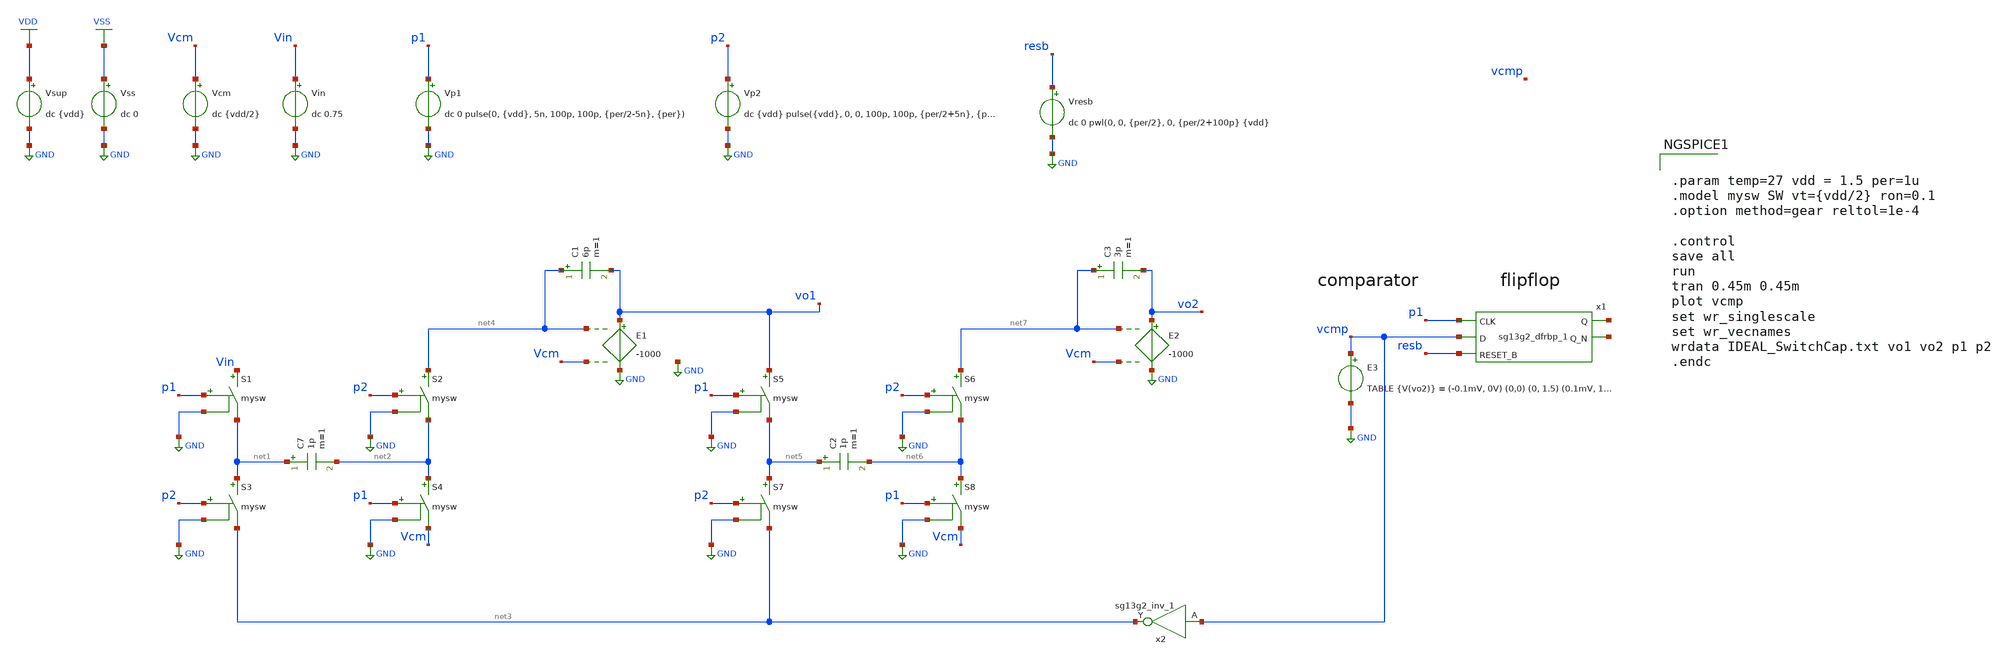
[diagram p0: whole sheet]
** sch_path: DSM/Schematics/Designs_Hrishi/IdealCircuits/IDEAL_DSM_VCCS.sch
**.subckt IDEAL_DSM_VCCS
Vcm Vcm GND dc {vdd/2}
Vin Vin GND dc 0.75
Vp1 p1 GND dc 0 pulse(0, {vdd}, 5n, 100p, 100p, {per/2-5n}, {per})
Vp2 p2 GND dc {vdd} pulse({vdd}, 0, 0, 100p, 100p, {per/2+5n}, {per})
S1 Vin net1 p1 GND mysw
S2 net4 net2 p2 GND mysw
S3 net1 net3 p2 GND mysw
S4 net2 Vcm p1 GND mysw
C7 net1 net2 1p m=1
C1 net4 vo1 6p m=1
S5 vo1 net5 p1 GND mysw
S6 net7 net6 p2 GND mysw
S7 net5 net3 p2 GND mysw
S8 net6 Vcm p1 GND mysw
C2 net5 net6 1p m=1
C3 net7 vo2 3p m=1
x2 net3 vcmp Vdd Vss sg13g2_inv_1
Vresb resb GND dc 0 pwl(0, 0, {per/2}, 0, {per/2+100p} {vdd}
Vsup VDD GND dc {vdd}
Vss VSS GND dc 0
E1 vo1 GND net4 Vcm -1000
E2 vo2 GND net7 Vcm -1000
E3 vcmp GND TABLE {V(vo2)} = (-0.1mV, 0V) (0,0) (0, 1.5) (0.1mV, 1.5)
x1 net8 net9 p1 vcmp resb VDD VSS sg13g2_dfrbp_1
**** begin user architecture code

.lib $::SG13G2_MODELS/cornerMOSlv.lib mos_tt
.lib $::SG13G2_MODELS/cornerRES.lib res_typ
.inc /foss/pdks/sg13g2/libs.ref/sg13g2_stdcell/spice/sg13g2_stdcell.spice



.param temp=27 vdd = 1.5 per=1u
.model mysw SW vt={vdd/2} ron=0.1
.option method=gear reltol=1e-4

.control
save all
run
tran 0.45m 0.45m
plot vcmp
set wr_singlescale
set wr_vecnames
wrdata IDEAL_SwitchCap.txt vo1 vo2 p1 p2
.endc


**** end user architecture code
**.ends

* expanding   symbol:  sg13g2_stdcells/sg13g2_inv_1.sym # of pins=2
** sym_path: sg13g2_stdcells/sg13g2_inv_1.sym
** sch_path: sg13g2_stdcells/sg13g2_inv_1.sch
.subckt sg13g2_inv_1 Y A VDD VSS
*.opin Y
*.ipin A
*.iopin VDD
*.iopin VSS
XM1 Y A VSS VSS sg13_lv_nmos w=740.00n l=130.00n ng=1 m=1 mm_ok=1
XM2 Y A VDD VDD sg13_lv_pmos w=1.12u l=130.00n ng=1 m=1 mm_ok=1
.ends


* expanding   symbol:  sg13g2_stdcells/sg13g2_dfrbp_1.sym # of pins=5
** sym_path: sg13g2_stdcells/sg13g2_dfrbp_1.sym
** sch_path: sg13g2_stdcells/sg13g2_dfrbp_1.sch
.subckt sg13g2_dfrbp_1 Q Q_N CLK D RESET_B VDD VSS
*.ipin D
*.ipin RESET_B
*.ipin CLK
*.opin Q
*.opin Q_N
*.iopin VDD
*.iopin VSS
XM1 Db D net10 VSS sg13_lv_nmos w=420.00n l=130.00n ng=1 m=1 mm_ok=1
XM2 net10 RESET_B VSS VSS sg13_lv_nmos w=420.00n l=130.00n ng=1 m=1 mm_ok=1
XM3 net1 clkneg net9 VSS sg13_lv_nmos w=420.00n l=130.00n ng=1 m=1 mm_ok=1
XM4 net9 net1 VSS VSS sg13_lv_nmos w=420.00n l=130.00n ng=1 m=1 mm_ok=1
XM5 net1 net1 net5 VSS sg13_lv_nmos w=420.00n l=130.00n ng=1 m=1 mm_ok=1
XM6 net5 RESET_B VSS VSS sg13_lv_nmos w=420.00n l=130.00n ng=1 m=1 mm_ok=1
XM7 Q_N net1 VSS VSS sg13_lv_nmos w=740.00n l=130.00n ng=1 m=1 mm_ok=1
XM8 net2 net1 VSS VSS sg13_lv_nmos w=740.00n l=130.00n ng=1 m=1 mm_ok=1
XM9 Q net2 VSS VSS sg13_lv_nmos w=740.00n l=130.00n ng=1 m=1 mm_ok=1
XM10 clkneg CLK VSS VSS sg13_lv_nmos w=740.00n l=130.00n ng=1 m=1 mm_ok=1
XM11 clkpos clkneg VSS VSS sg13_lv_nmos w=740.00n l=130.00n ng=1 m=1 mm_ok=1
XM12 Db clkneg net3 VSS sg13_lv_nmos w=420.00n l=130.00n ng=1 m=1 mm_ok=1
XM13 net3 clkpos net8 VSS sg13_lv_nmos w=420.00n l=130.00n ng=1 m=1 mm_ok=1
XM14 net8 net3 net4 VSS sg13_lv_nmos w=420.00n l=130.00n ng=1 m=1 mm_ok=1
XM15 net4 RESET_B VSS VSS sg13_lv_nmos w=420.00n l=130.00n ng=1 m=1 mm_ok=1
XM16 net3 net3 VSS VSS sg13_lv_nmos w=740.00n l=130.00n ng=1 m=1 mm_ok=1
XM17 net3 clkpos net1 VSS sg13_lv_nmos w=740.00n l=130.00n ng=1 m=1 mm_ok=1
XM18 Db RESET_B VDD VDD sg13_lv_pmos w=420.00n l=130.00n ng=1 m=1 mm_ok=1
XM19 Db D VDD VDD sg13_lv_pmos w=420.00n l=130.00n ng=1 m=1 mm_ok=1
XM20 net7 net1 VDD VDD sg13_lv_pmos w=420.00n l=130.00n ng=1 m=1 mm_ok=1
XM21 net1 clkpos net7 VDD sg13_lv_pmos w=420.00n l=130.00n ng=1 m=1 mm_ok=1
XM22 net1 net1 VDD VDD sg13_lv_pmos w=420.00n l=130.00n ng=1 m=1 mm_ok=1
XM23 net1 RESET_B VDD VDD sg13_lv_pmos w=420.00n l=130.00n ng=1 m=1 mm_ok=1
XM24 Q_N net1 VDD VDD sg13_lv_pmos w=1.12u l=130.00n ng=1 m=1 mm_ok=1
XM25 net2 net1 VDD VDD sg13_lv_pmos w=1.12u l=130.00n ng=1 m=1 mm_ok=1
XM26 Q net2 VDD VDD sg13_lv_pmos w=1.12u l=130.00n ng=1 m=1 mm_ok=1
XM27 clkneg CLK VDD VDD sg13_lv_pmos w=1.12u l=130.00n ng=1 m=1 mm_ok=1
XM28 clkpos clkneg VDD VDD sg13_lv_pmos w=1.12u l=130.00n ng=1 m=1 mm_ok=1
XM29 Db clkpos net3 VDD sg13_lv_pmos w=420.00n l=130.00n ng=1 m=1 mm_ok=1
XM30 net6 net3 VDD VDD sg13_lv_pmos w=420.00n l=130.00n ng=1 m=1 mm_ok=1
XM31 net3 clkneg net6 VDD sg13_lv_pmos w=420.00n l=130.00n ng=1 m=1 mm_ok=1
XM32 net3 RESET_B VDD VDD sg13_lv_pmos w=420.00n l=130.00n ng=1 m=1 mm_ok=1
XM33 net3 net3 VDD VDD sg13_lv_pmos w=1.000u l=130.00n ng=1 m=1 mm_ok=1
XM34 net3 clkneg net1 VDD sg13_lv_pmos w=1.000u l=130.00n ng=1 m=1 mm_ok=1
.ends

.GLOBAL GND
.GLOBAL VDD
.GLOBAL VSS
.end
